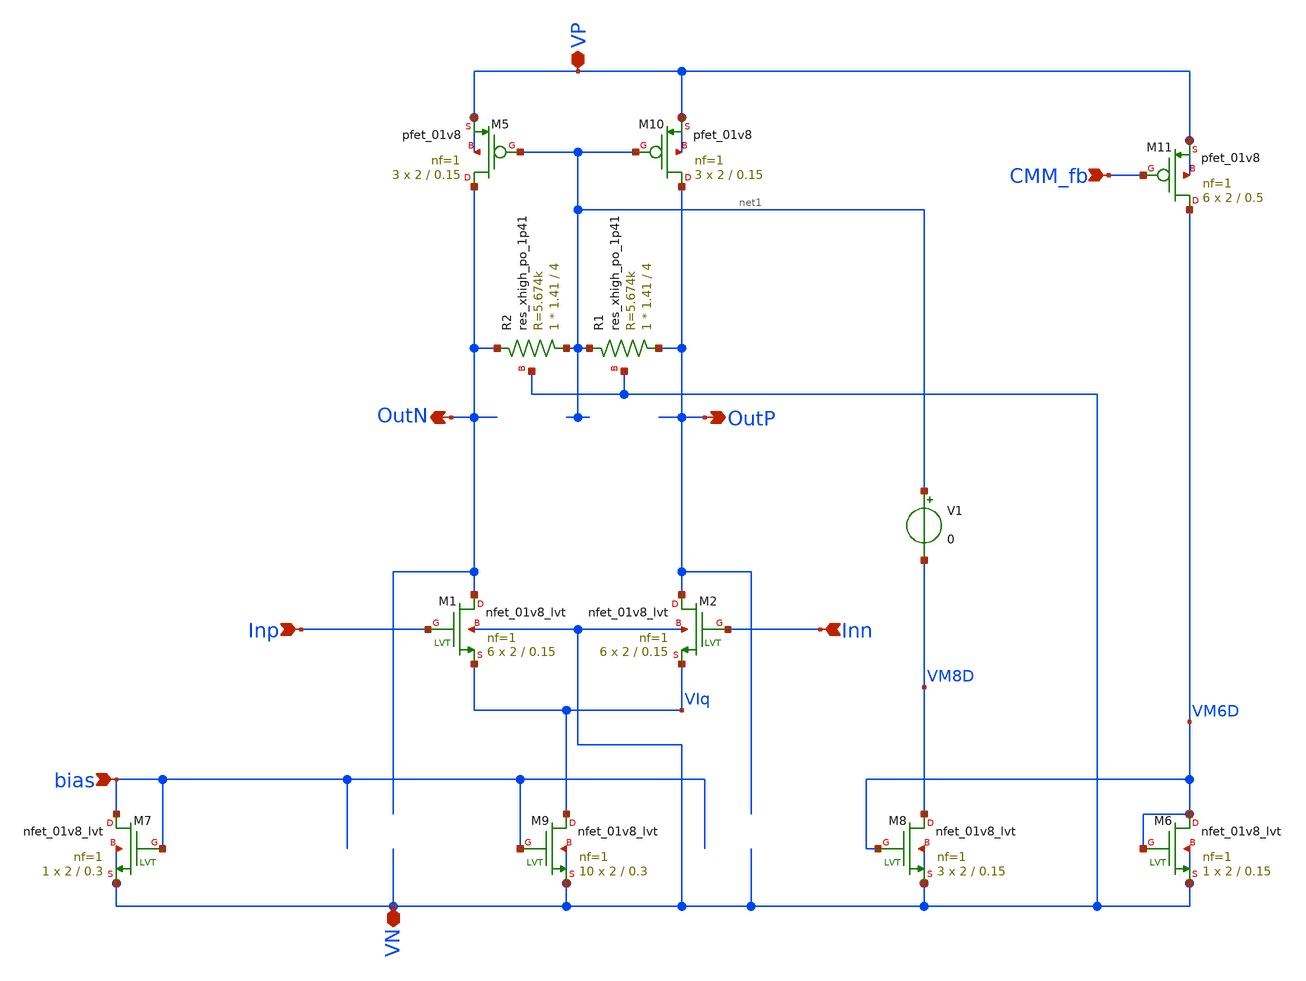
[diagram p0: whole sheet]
** sch_path: xschem/comp/comp_adv2.sch
**.subckt comp_adv2 Inp bias Inn VP VN OutN OutP CMM_fb
*.ipin Inp
*.ipin bias
*.ipin Inn
*.iopin VP
*.iopin VN
*.opin OutN
*.opin OutP
*.ipin CMM_fb
XM1 OutN Inp VIq VN sky130_fd_pr__nfet_01v8_lvt L=0.15 W=2 nf=1 ad='int((nf+1)/2) * W/nf * 0.29' as='int((nf+2)/2) * W/nf * 0.29'
+ pd='2*int((nf+1)/2) * (W/nf + 0.29)' ps='2*int((nf+2)/2) * (W/nf + 0.29)' nrd='0.29 / W' nrs='0.29 / W'
+ sa=0 sb=0 sd=0 mult=6 m=6
XM2 OutP Inn VIq VN sky130_fd_pr__nfet_01v8_lvt L=0.15 W=2 nf=1 ad='int((nf+1)/2) * W/nf * 0.29' as='int((nf+2)/2) * W/nf * 0.29'
+ pd='2*int((nf+1)/2) * (W/nf + 0.29)' ps='2*int((nf+2)/2) * (W/nf + 0.29)' nrd='0.29 / W' nrs='0.29 / W'
+ sa=0 sb=0 sd=0 mult=6 m=6
XM7 bias bias VN VN sky130_fd_pr__nfet_01v8_lvt L=0.3 W=2 nf=1 ad='int((nf+1)/2) * W/nf * 0.29' as='int((nf+2)/2) * W/nf * 0.29'
+ pd='2*int((nf+1)/2) * (W/nf + 0.29)' ps='2*int((nf+2)/2) * (W/nf + 0.29)' nrd='0.29 / W' nrs='0.29 / W'
+ sa=0 sb=0 sd=0 mult=1 m=1
XM9 VIq bias VN VN sky130_fd_pr__nfet_01v8_lvt L=0.3 W=2 nf=1 ad='int((nf+1)/2) * W/nf * 0.29' as='int((nf+2)/2) * W/nf * 0.29'
+ pd='2*int((nf+1)/2) * (W/nf + 0.29)' ps='2*int((nf+2)/2) * (W/nf + 0.29)' nrd='0.29 / W' nrs='0.29 / W'
+ sa=0 sb=0 sd=0 mult=10 m=10
XM8 VM8D VM6D VN VN sky130_fd_pr__nfet_01v8_lvt L=0.15 W=2 nf=1 ad='int((nf+1)/2) * W/nf * 0.29' as='int((nf+2)/2) * W/nf * 0.29'
+ pd='2*int((nf+1)/2) * (W/nf + 0.29)' ps='2*int((nf+2)/2) * (W/nf + 0.29)' nrd='0.29 / W' nrs='0.29 / W'
+ sa=0 sb=0 sd=0 mult=3 m=3
XM5 OutN net1 VP VP sky130_fd_pr__pfet_01v8 L=0.15 W=2 nf=1 ad='int((nf+1)/2) * W/nf * 0.29' as='int((nf+2)/2) * W/nf * 0.29'
+ pd='2*int((nf+1)/2) * (W/nf + 0.29)' ps='2*int((nf+2)/2) * (W/nf + 0.29)' nrd='0.29 / W' nrs='0.29 / W'
+ sa=0 sb=0 sd=0 mult=3 m=3
XM10 OutP net1 VP VP sky130_fd_pr__pfet_01v8 L=0.15 W=2 nf=1 ad='int((nf+1)/2) * W/nf * 0.29' as='int((nf+2)/2) * W/nf * 0.29'
+ pd='2*int((nf+1)/2) * (W/nf + 0.29)' ps='2*int((nf+2)/2) * (W/nf + 0.29)' nrd='0.29 / W' nrs='0.29 / W'
+ sa=0 sb=0 sd=0 mult=3 m=3
XM6 VM6D VM6D VN VN sky130_fd_pr__nfet_01v8_lvt L=0.15 W=2 nf=1 ad='int((nf+1)/2) * W/nf * 0.29' as='int((nf+2)/2) * W/nf * 0.29'
+ pd='2*int((nf+1)/2) * (W/nf + 0.29)' ps='2*int((nf+2)/2) * (W/nf + 0.29)' nrd='0.29 / W' nrs='0.29 / W'
+ sa=0 sb=0 sd=0 mult=1 m=1
XM11 VM6D CMM_fb VP VP sky130_fd_pr__pfet_01v8 L=0.5 W=2 nf=1 ad='int((nf+1)/2) * W/nf * 0.29' as='int((nf+2)/2) * W/nf * 0.29'
+ pd='2*int((nf+1)/2) * (W/nf + 0.29)' ps='2*int((nf+2)/2) * (W/nf + 0.29)' nrd='0.29 / W' nrs='0.29 / W'
+ sa=0 sb=0 sd=0 mult=6 m=6
V1 net1 VM8D 0
XR1 OutP net1 VN sky130_fd_pr__res_xhigh_po_1p41 L=4 mult=1 m=1
XR2 net1 OutN VN sky130_fd_pr__res_xhigh_po_1p41 L=4 mult=1 m=1
**** begin user architecture code

*.lib $::SKYWATER_MODELS/sky130.lib.spice tt
.lib $::SKYWATER_MODELS/sky130.lib.spice.tt.red tt



*.options savecurrents
.option warn=1
.control
set wr_vecnames
set wr_singlescale
* Power consumption
op
* save all
* #OP#
print @m.xm1.msky130_fd_pr__nfet_01v8_lvt[gds]
print vdd#branch
print v(vm2d)
print v(vm3d)
print v(UD_M5)
wrdata 'result_op.csv' vdd#branch
ac dec 10 1 10G
meas ac dc_gain_vm2d FIND vdb(vm2d) AT=1
let bw_amp_vm2d=dc_gain_vm2d-3
meas ac dc_gain_vm3d FIND vdb(vm3d) AT=1
let bw_amp_vm3d=dc_gain_vm3d-3
meas ac bw_vm2d when vdb(vm2d)=bw_amp_vm2d
meas ac bw_vm3d when vdb(vm3d)=bw_amp_vm3d
*MEAS AC phasem FIND vp(vm2d) WHEN vdb(vm2d)=0
* wrdata 'result_ac.csv' dc_gain bw
* plot vdb(vm2D) log
*
*print WM3D
run
reset
save @m.xm1.msky130_fd_pr__nfet_01v8_lvt[gds]
save @m.xm1.msky130_fd_pr__nfet_01v8_lvt[gm]
save @m.xm1.msky130_fd_pr__nfet_01v8_lvt[cgs]
save @m.xm1.msky130_fd_pr__nfet_01v8_lvt[cdg]
save @m.xm2.msky130_fd_pr__nfet_01v8_lvt[gm]
save @m.xm2.msky130_fd_pr__nfet_01v8_lvt[gds]
save @m.xm2.msky130_fd_pr__nfet_01v8_lvt[cgs]
save @m.xm2.msky130_fd_pr__nfet_01v8_lvt[cdg]
save @m.xm3.msky130_fd_pr__nfet_01v8_lvt[gm]
save @m.xm3.msky130_fd_pr__nfet_01v8_lvt[gds]
save @m.xm3.msky130_fd_pr__nfet_01v8_lvt[cgs]
save @m.xm3.msky130_fd_pr__nfet_01v8_lvt[cdg]
save @m.xm4.msky130_fd_pr__nfet_01v8_lvt[gm]
save @m.xm4.msky130_fd_pr__nfet_01v8_lvt[gds]
save @m.xm4.msky130_fd_pr__nfet_01v8_lvt[cgs]
save @m.xm4.msky130_fd_pr__nfet_01v8_lvt[cdg]
save @m.xm5.msky130_fd_pr__pfet_01v8_lvt[gm]
save @m.xm5.msky130_fd_pr__pfet_01v8_lvt[gds]
save @m.xm5.msky130_fd_pr__pfet_01v8_lvt[cgs]
save @m.xm5.msky130_fd_pr__pfet_01v8_lvt[cdg]
save @m.xm6.msky130_fd_pr__pfet_01v8_lvt[gm]
save @m.xm6.msky130_fd_pr__pfet_01v8_lvt[gds]
save @m.xm6.msky130_fd_pr__pfet_01v8_lvt[cgs]
save @m.xm6.msky130_fd_pr__pfet_01v8_lvt[cdg]
save @m.xm7.msky130_fd_pr__nfet_01v8_lvt[gm]
save @m.xm7.msky130_fd_pr__nfet_01v8_lvt[gds]
save @m.xm7.msky130_fd_pr__nfet_01v8_lvt[cgs]
save @m.xm7.msky130_fd_pr__nfet_01v8_lvt[cdg]
save @m.xm8.msky130_fd_pr__nfet_01v8_lvt[gm]
save @m.xm8.msky130_fd_pr__nfet_01v8_lvt[gds]
save @m.xm8.msky130_fd_pr__nfet_01v8_lvt[cgs]
save @m.xm8.msky130_fd_pr__nfet_01v8_lvt[cdg]
save @m.xm9.msky130_fd_pr__nfet_01v8_lvt[gm]
save @m.xm9.msky130_fd_pr__nfet_01v8_lvt[gds]
save @m.xm9.msky130_fd_pr__nfet_01v8_lvt[cgs]
save @m.xm9.msky130_fd_pr__nfet_01v8_lvt[cdg]
save v(Voutp)
save v(Voutn)
save v(VIa)
save v(VIq)

save v(Vinn)
save v(Vinp)
save v(VM8G)

op
write comp.raw
run
*reset
*noise v(vm1d) I1 dec 100 1 10G
*print all
*setplot noise2
*write noise2.raw
*run
reset
ac dec 10 1 1T
plot vdb(Voutp) vdb(Voutn)
plot phase(Voutp)/pi*180 phase(Voutn)/pi*180
run
reset
tran 1ps 10ns
plot v(Vinp) v(Voutn) v(Voutp)
run
.endc


**** end user architecture code
**.ends
.end
